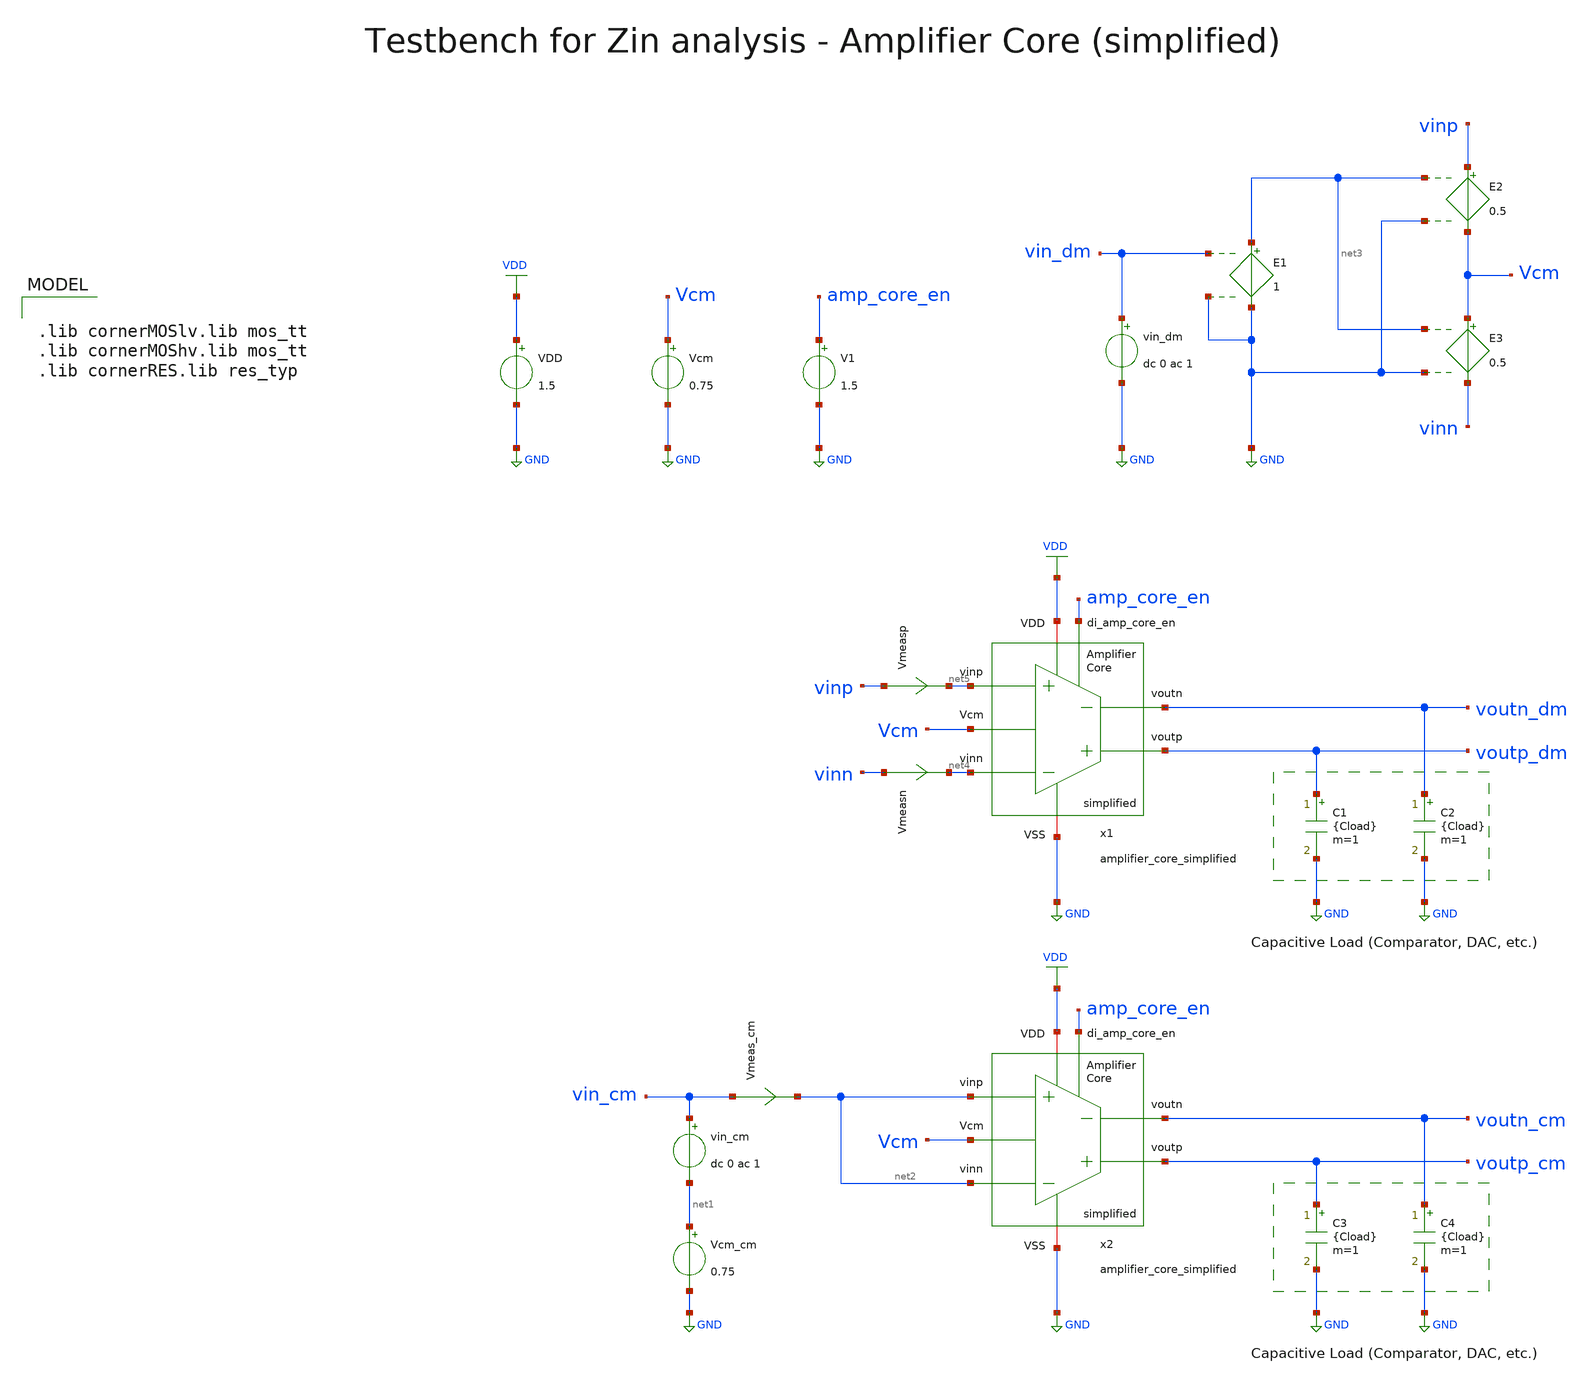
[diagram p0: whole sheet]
** sch_path: SG13G2_ATBS-ADC-main/xschem/bio_amplifier/amplifier_core/testbenches/amplifier_core_simplified_tb_Zin.sch
**.subckt amplifier_core_simplified_tb_Zin
VDD VDD GND 1.5
C1 voutp_dm GND {Cload} m=1
C2 voutn_dm GND {Cload} m=1
Vcm Vcm GND 0.75
V1 amp_core_en GND 1.5
x1 voutp_dm voutn_dm amp_core_en net4 net5 VDD GND Vcm amplifier_core_simplified
C3 voutp_cm GND {Cload} m=1
C4 voutn_cm GND {Cload} m=1
x2 voutp_cm voutn_cm amp_core_en net2 net2 VDD GND Vcm amplifier_core_simplified
vin_cm vin_cm net1 dc 0 ac 1
Vmeasp vinp net5 0
.save i(vmeasp)
Vmeasn vinn net4 0
.save i(vmeasn)
Vmeas_cm vin_cm net2 0
.save i(vmeas_cm)
Vcm_cm net1 GND 0.75
E3 Vcm vinn net3 GND 0.5
E2 vinp Vcm net3 GND 0.5
E1 net3 GND vin_dm GND 1
vin_dm vin_dm GND dc 0 ac 1
**** begin user architecture code


.param temp=27
* 228fF DAC + (1 - beta) * 3.3pF
.param Cload=3.49p
.options savecurrents reltol=1e-2 abstol=1e-15 gmin=1e-15 rshunt=1e15
.control

save v(vinp) v(vinn) i(Vmeasp) i(Vmeasn) v(vin_cm) i(Vmeas_cm)

set wr_vecnames
set wr_singlescale

* User Constants
let f_min = 10m
let f_max = 100
let fdc = 10

* Operating Point Analysis
op
remzerovec
write amplifier_core_simplified_tb_Zin.raw
set appendwrite

* AC Analysis
ac dec 101 $&const.f_min $&const.f_max
remzerovec
write amplifier_core_simplified_tb_Zin.raw

* Plotting Differential Mode Zin
* let Zin_dm = (v(vinp) - v(vinn)) / (i(Vmeasp) - i(Vmeasn))
* let Zin_dm = (v(vinp) - v(vinn)) / (i(Vmeasp) + i(Vmeasn))
let Zin_dm = (v(vinp) - v(vinn)) / i(Vmeasp)
plot Zin_dm ylabel 'DM Zin'

* Plotting Common Mode Zin
let Zin_cm = v(vin_cm) / i(Vmeas_cm)
plot Zin_cm ylabel 'CM Zin'

* Measurements
meas ac Zindc_dm find Zin_dm when frequency = fdc
print Zindc_dm

meas ac Zindc_cm find Zin_cm when frequency = fdc
print Zindc_cm

* Write Data
set wr_vecnames
set wr_singlescale
wrdata
+ /foss/designs/SG13G2_ATBS-ADC-main/python/plot_simulations/data/amplifier_core_simplified_tb_Zin.txt v(Zin_dm) v(Zin_cm)

*quit
.endc



.lib cornerMOSlv.lib mos_tt
.lib cornerMOShv.lib mos_tt
.lib cornerRES.lib res_typ

**** end user architecture code
**.ends
.GLOBAL GND
.GLOBAL VDD
.end
